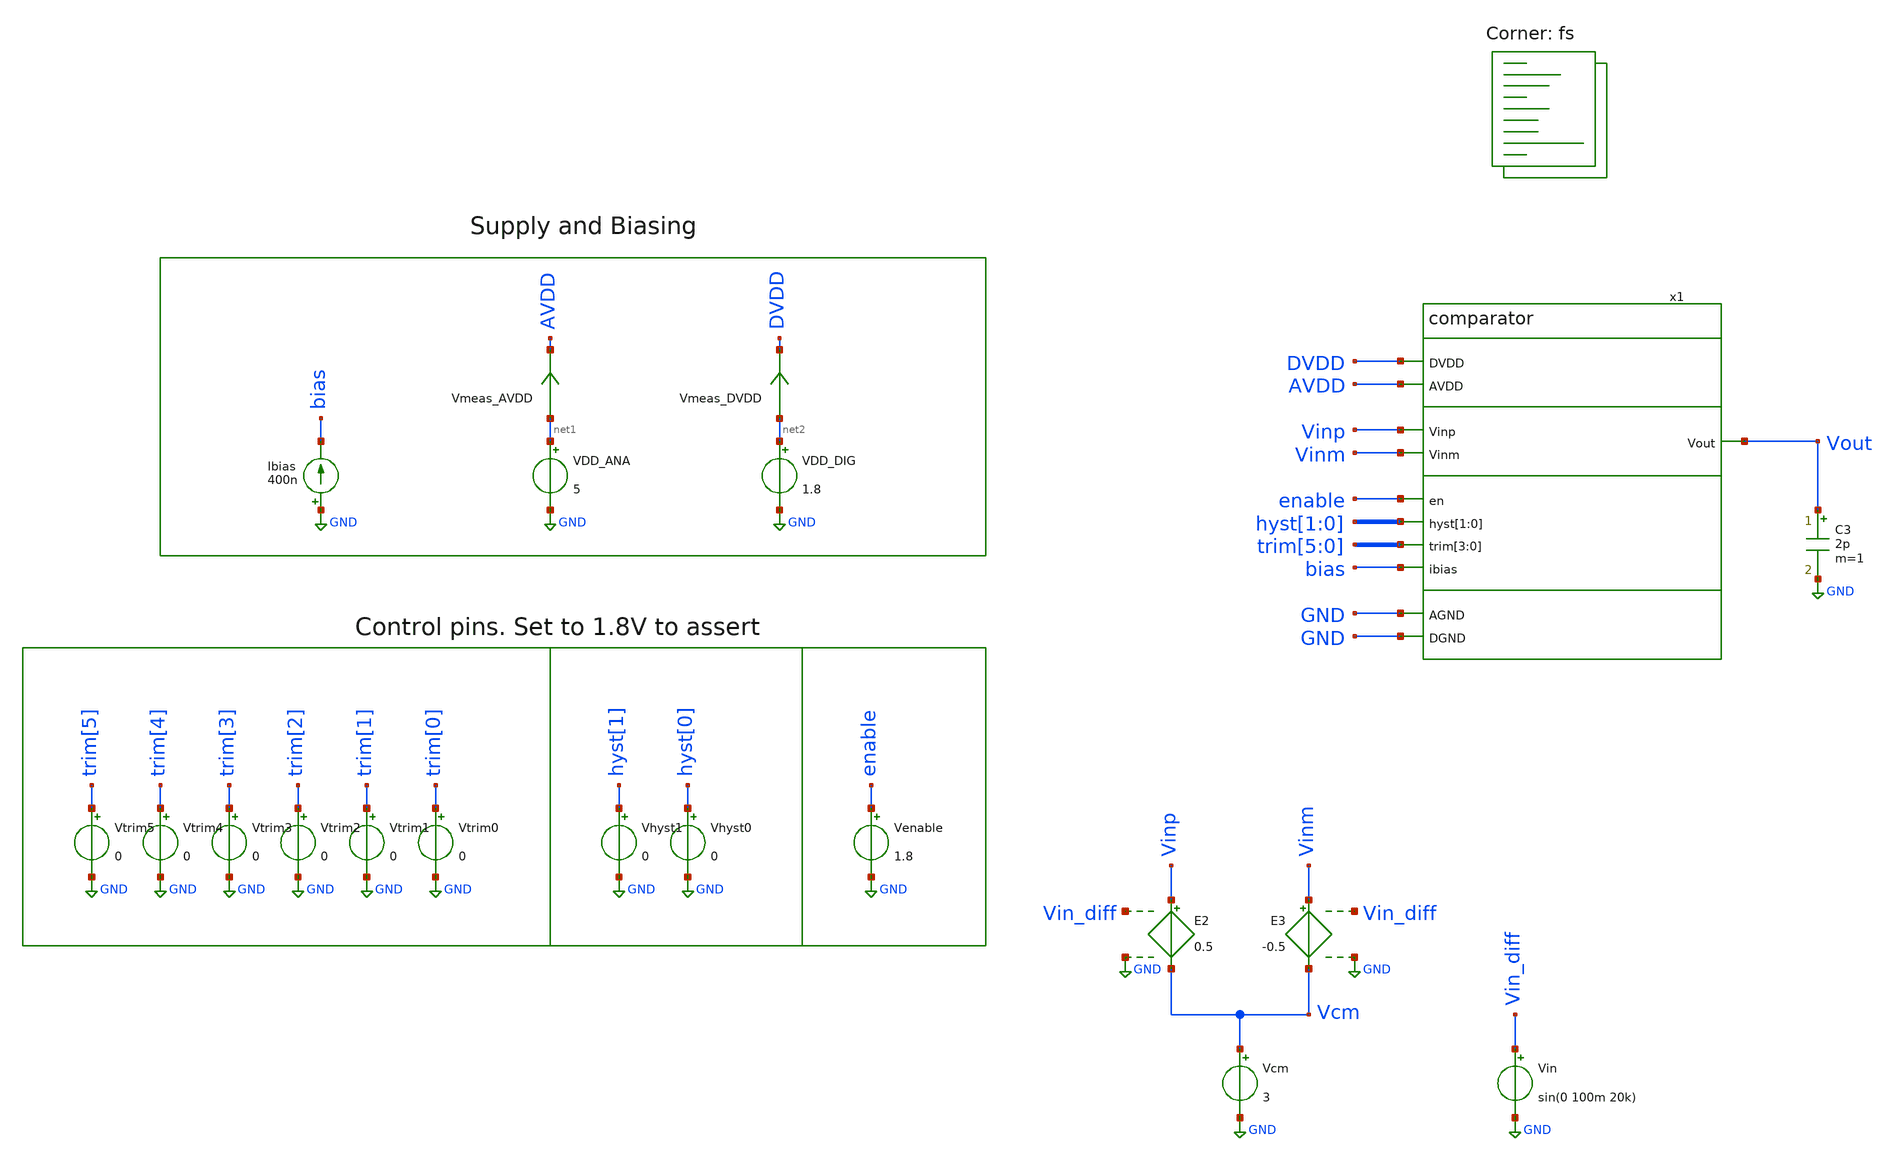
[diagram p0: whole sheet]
** sch_path: xschem/tb_comparator_bandwidth.sch
**.subckt tb_comparator_bandwidth
VDD_ANA net1 GND 5
VDD_DIG net2 GND 1.8
Ibias GND bias 400n
C3 Vout GND 2p m=1
Vmeas_AVDD net1 AVDD 0
.save i(vmeas_avdd)
Vmeas_DVDD net2 DVDD 0
.save i(vmeas_dvdd)
Vcm Vcm GND 3
Vin Vin_diff GND sin(0 100m 20k)
E2 Vinp Vcm Vin_diff GND 0.5
E3 Vinm Vcm Vin_diff GND -0.5
Vtrim3 trim[3] GND 0
Vtrim2 trim[2] GND 0
Vtrim1 trim[1] GND 0
Vtrim0 trim[0] GND 0
Vhyst1 hyst[1] GND 0
Vhyst0 hyst[0] GND 0
Venable enable GND 1.8
Vtrim5 trim[5] GND 0
Vtrim4 trim[4] GND 0
x1 DVDD AVDD GND GND Vinp Vout Vinm enable hyst[1] hyst[0] trim[5] trim[4] trim[3] trim[2] bias
+ comparator
**** begin user architecture code
.lib $::SKYWATER_MODELS/sky130.lib.spice fs


*.save v(vout) i(e3)
.save all
.tran 10n 140u 40u
.control
set plotstr = ' '
set writestr = ' '

let i = 0
foreach temp_val -40 27 85
   set temp=$temp_val
   foreach vdd_ana_val 2.95 3.3 5.5
      alter VDD_ANA $vdd_ana_val
      foreach vcm_val 0.1 {$vdd_ana_val*0.25} {$vdd_ana_val/2} {$vdd_ana_val*0.75} {-0.1+$vdd_ana_val}
         alter Vcm $vcm_val
         foreach ibias_val 400n
            alter ibias $ibias_val
            run
            set plotstr = ( $plotstr {$curplot}.v(vout) )
            set writestr = ( $writestr {$curplot}.v(vout) )
            let i = i+1
         end
      end
   end
end
plot $plotstr
set filetype = ascii
wrdata results_bandwidth_fs.out $writestr
.endc


**** end user architecture code
**.ends
.GLOBAL GND
.end
